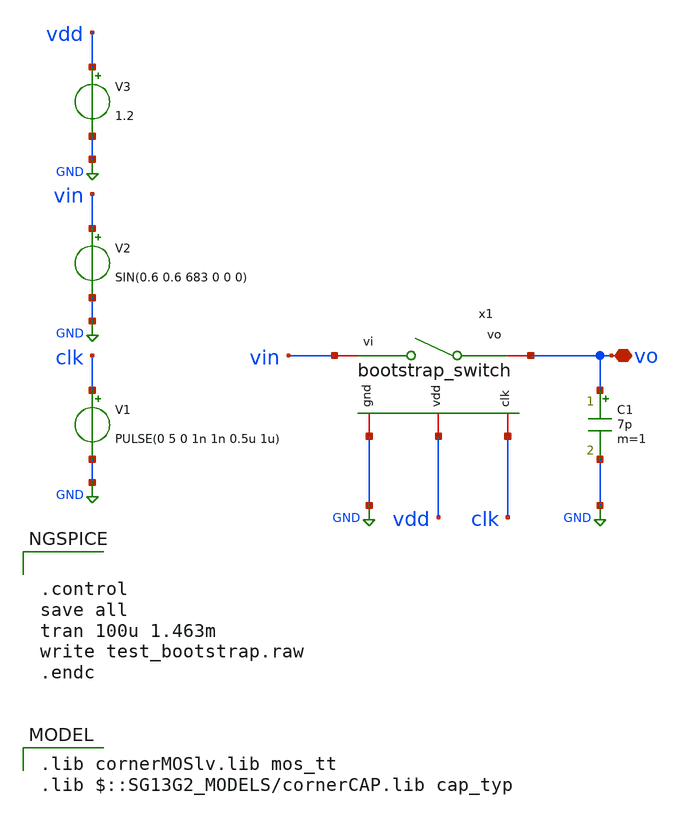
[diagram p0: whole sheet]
** sch_path: modules/module_3_8_bit_SAR_ADC/part_2_digital_comps/bootstrap_switch/testbench/bootstrap_switch_tbs.sch
**.subckt bootstrap_switch_tbs vo
*.iopin vo
x1 vdd vin vo clk GND bootstrap_switch
V1 clk GND PULSE(0 5 0 1n 1n 0.5u 1u)
V2 vin GND SIN(0.6 0.6 683 0 0 0)
V3 vdd GND 1.2
C1 vo GND 7p m=1
**** begin user architecture code
 .lib cornerMOSlv.lib mos_tt
.lib $::SG13G2_MODELS/cornerCAP.lib cap_typ



.control
save all
tran 100u 1.463m
write test_bootstrap.raw
.endc


**** end user architecture code
**.ends

* expanding   symbol:
*+  /home/pedersen/projects/IHP-AnalogAcademy/modules/module_3_8_bit_SAR_ADC/part_2_digital_comps/bootstrap_switch/schematic/bootstrap_switch.sym # of pins=5
** sym_path: modules/module_3_8_bit_SAR_ADC/part_2_digital_comps/bootstrap_switch/schematic/bootstrap_switch.sym
** sch_path: modules/module_3_8_bit_SAR_ADC/part_2_digital_comps/bootstrap_switch/schematic/bootstrap_switch.sch
.subckt bootstrap_switch vdd vi vo clk gnd
*.iopin gnd
*.iopin vdd
*.iopin vi
*.iopin vo
*.iopin clk
XM1 vdd net2 net1 gnd sg13_lv_nmos w=1.3u l=0.13u ng=1 m=1 mm_ok=1
XM3 vdd net1 net2 gnd sg13_lv_nmos w=1.3u l=0.13u ng=1 m=1 mm_ok=1
XM4 net7 net10 net3 net3 sg13_lv_pmos w=500n l=0.13u ng=1 m=1 mm_ok=1
XM2 vdd net2 net3 gnd sg13_lv_nmos w=1.3u l=0.13u ng=1 m=1 mm_ok=1
XM6 net5 gp vdd vdd sg13_lv_pmos w=500n l=130n ng=1 m=1 mm_ok=1
XM5 net5 vdd net4 gnd sg13_lv_nmos w=3u l=0.13u ng=1 m=1 mm_ok=1
XM7 net4 clk_not gnd gnd sg13_lv_nmos w=3u l=0.13u ng=1 m=1 mm_ok=1
XC5 net2 clk_not cap_cmim w=4.665e-6 l=6.99e-6 m=1 mm_ok=1
XC6 net3 net6 cap_cmim w=11.485e-6 l=11.485e-6 m=1 mm_ok=1
XM8 net6 net5 vi gnd sg13_lv_nmos w=5u l=0.13u ng=1 m=1 mm_ok=1
XM9 vo net7 vi gnd sg13_lv_nmos w=5u l=0.13u ng=1 m=1 mm_ok=1
XM10 net8 vdd net7 gnd sg13_lv_nmos w=500n l=0.13u ng=1 m=1 mm_ok=1
XM11 gnd clk_not net8 gnd sg13_lv_nmos w=500n l=0.13u ng=1 m=1 mm_ok=1
XM12 net6 clk_not gnd gnd sg13_lv_nmos w=1.3u l=0.13u ng=1 m=1 mm_ok=1
XC1 net1 net9 cap_cmim w=4.665e-6 l=6.99e-6 m=1 mm_ok=1
x1 vdd clk_not net9 gnd inverter
x2 vdd gp net10 gnd inverter
x3 vdd clk clk_not gnd inverter
.ends


* expanding   symbol:
*+  /home/pedersen/projects/IHP-AnalogAcademy/modules/module_3_8_bit_SAR_ADC/part_2_digital_comps/bootstrap_switch/schematic/inverter.sym # of pins=4
** sym_path: modules/module_3_8_bit_SAR_ADC/part_2_digital_comps/bootstrap_switch/schematic/inverter.sym
** sch_path: modules/module_3_8_bit_SAR_ADC/part_2_digital_comps/bootstrap_switch/schematic/inverter.sch
.subckt inverter vdd vi vo gnd
*.iopin vi
*.iopin vo
*.iopin gnd
*.iopin vdd
XM5 vo vi vdd vdd sg13_lv_pmos w=800n l=130n ng=1 m=1 mm_ok=1
XM7 vo vi gnd gnd sg13_lv_nmos w=400n l=130n ng=1 m=1 mm_ok=1
.ends

.GLOBAL GND
.end
